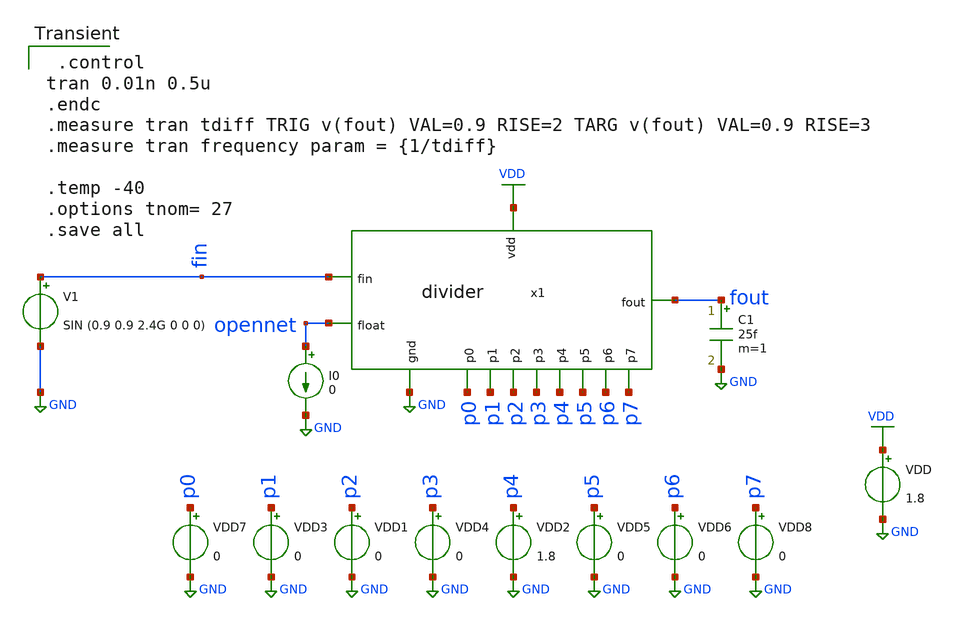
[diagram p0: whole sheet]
** sch_path: pll/dividers_lib/divider_tb/xschem/divider_tb.sch
**.subckt divider_tb
VDD VDD GND 1.8
VDD1 p2 GND 0
VDD2 p4 GND 1.8
VDD3 p1 GND 0
VDD4 p3 GND 0
VDD5 p5 GND 0
VDD6 p6 GND 0
VDD7 p0 GND 0
VDD8 p7 GND 0
x1 VDD fout GND p2 p7 p1 p6 p5 p4 p3 p0 fin opennet divider
V1 fin GND SIN (0.9 0.9 2.4G 0 0 0)
C1 fout GND 25f m=1
I0 opennet GND 0
**** begin user architecture code

** opencircuitdesign pdks install
.lib $::SKYWATER_MODELS/sky130.lib.spice tt



 .control
tran 0.01n 0.5u
.endc
.measure tran tdiff TRIG v(fout) VAL=0.9 RISE=2 TARG v(fout) VAL=0.9 RISE=3
.measure tran frequency param = {1/tdiff}

.temp -40
.options tnom= 27
.save all

**** end user architecture code
**.ends
.GLOBAL VDD
.GLOBAL GND
.end
